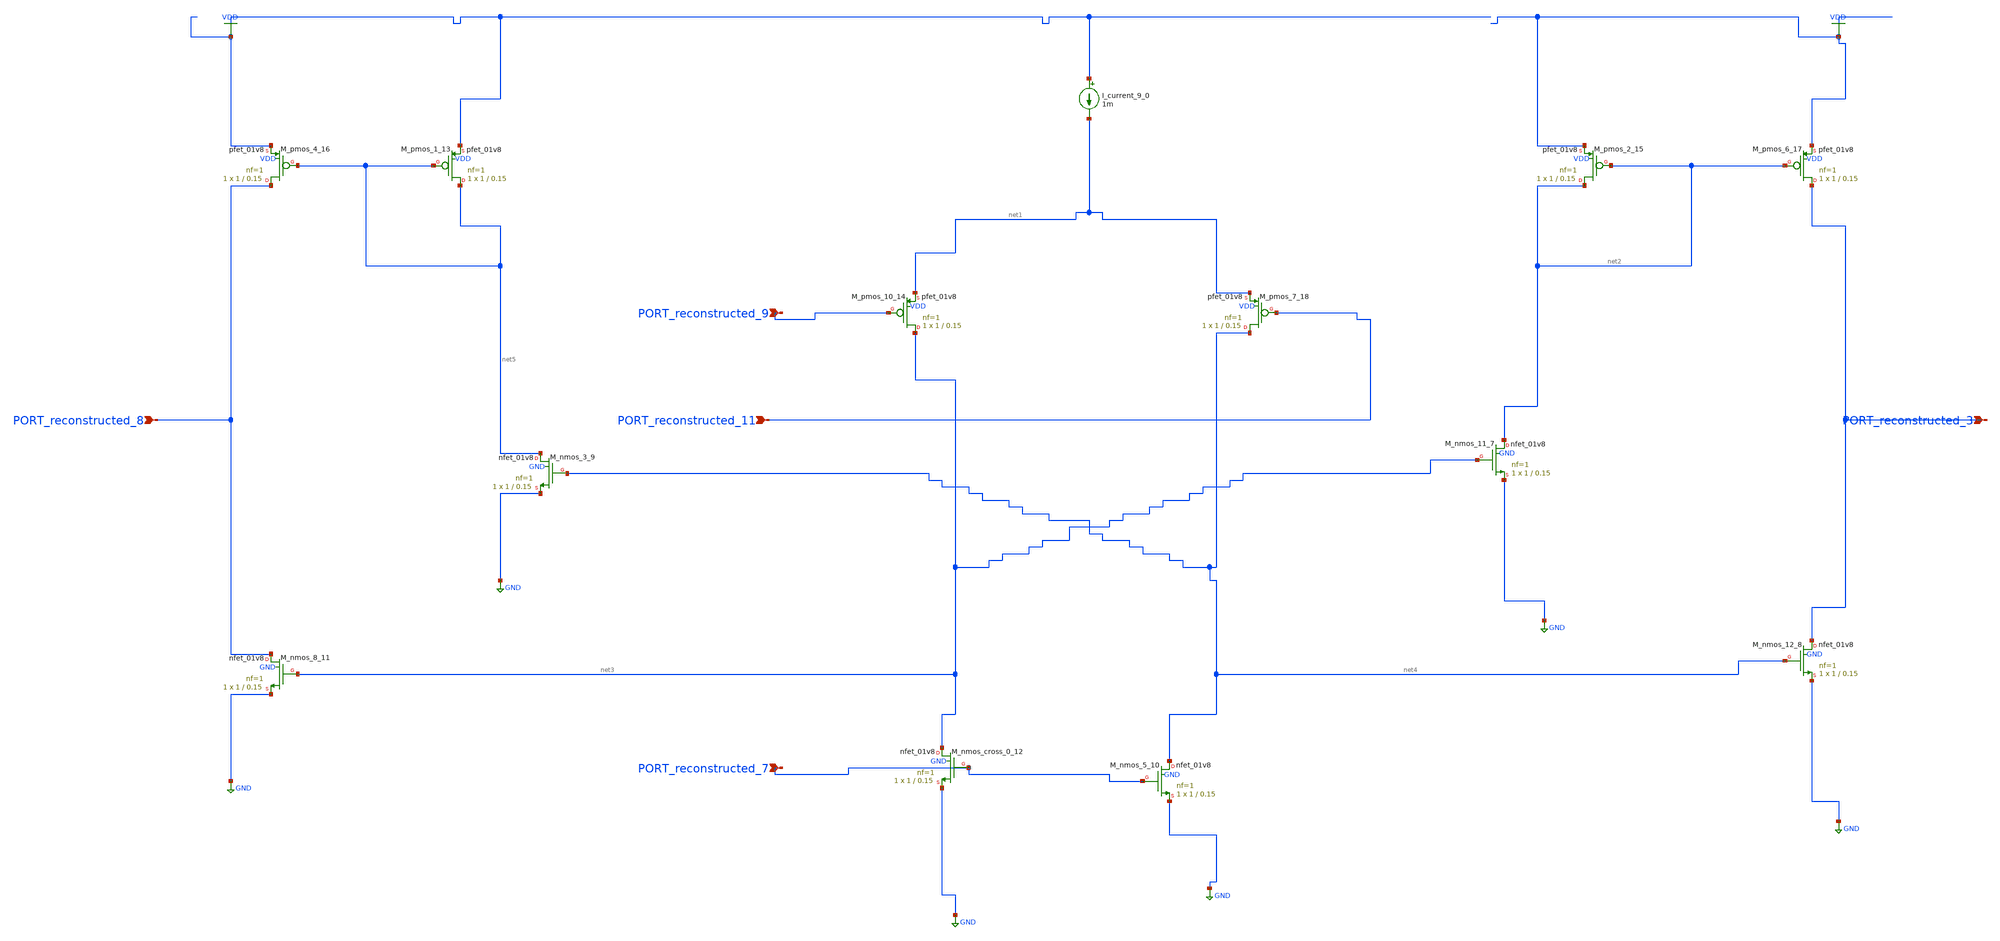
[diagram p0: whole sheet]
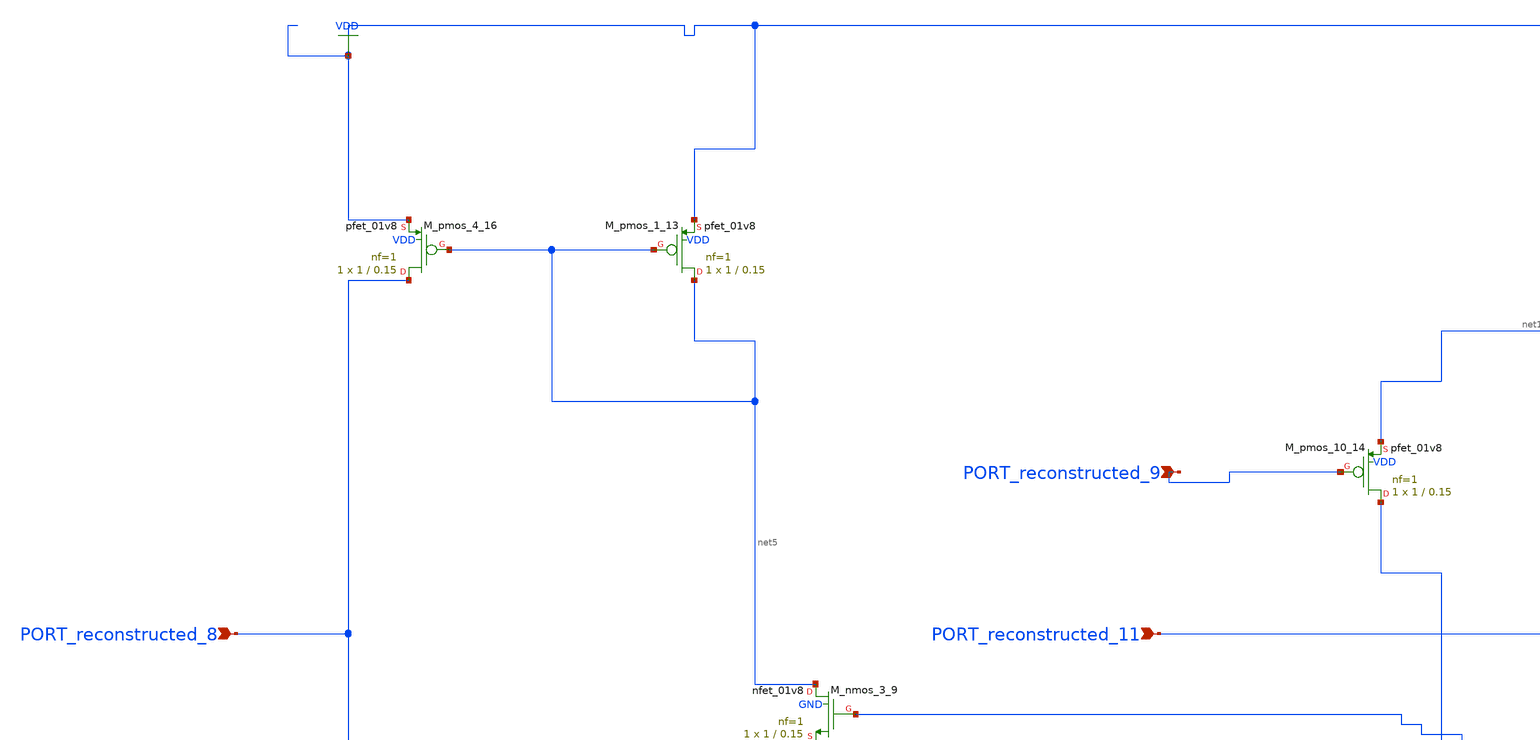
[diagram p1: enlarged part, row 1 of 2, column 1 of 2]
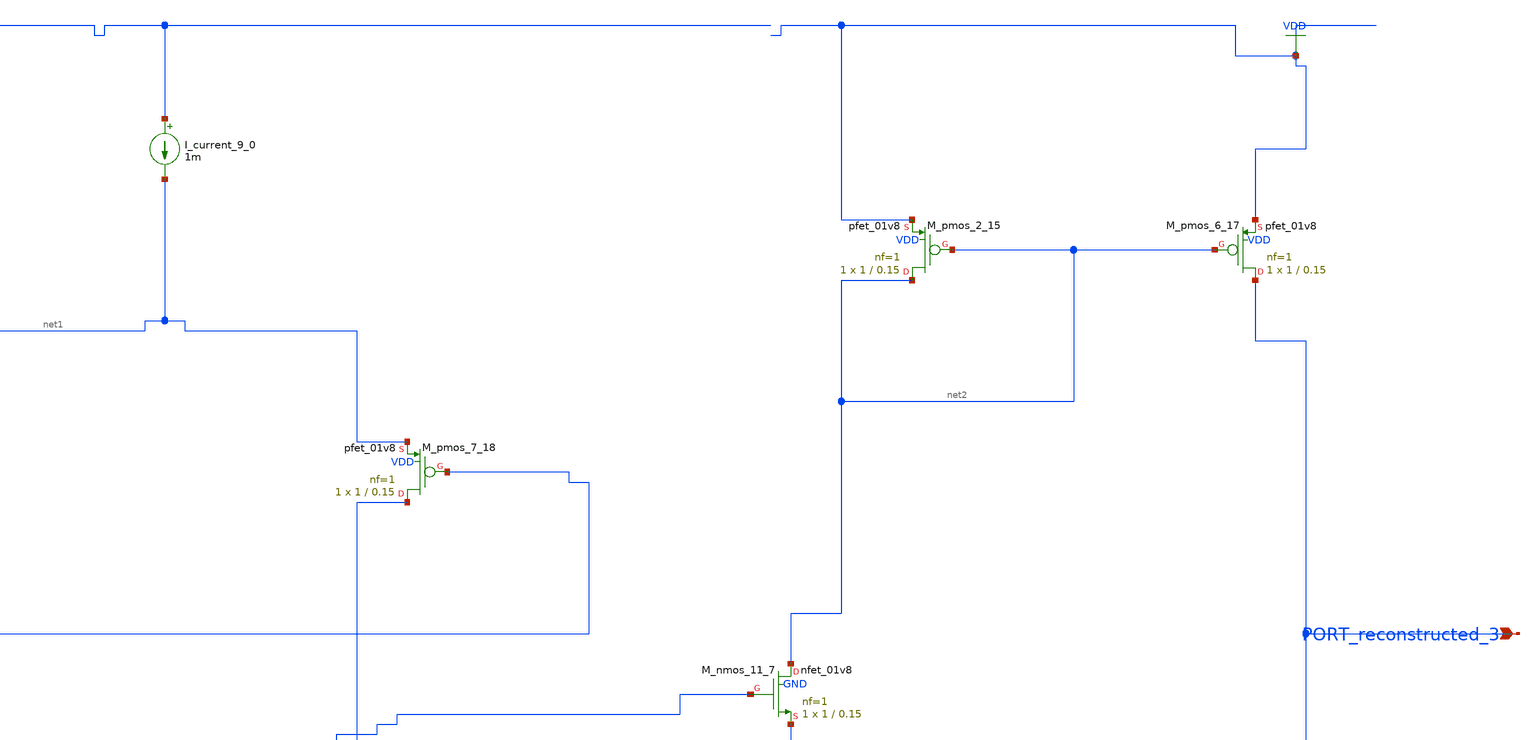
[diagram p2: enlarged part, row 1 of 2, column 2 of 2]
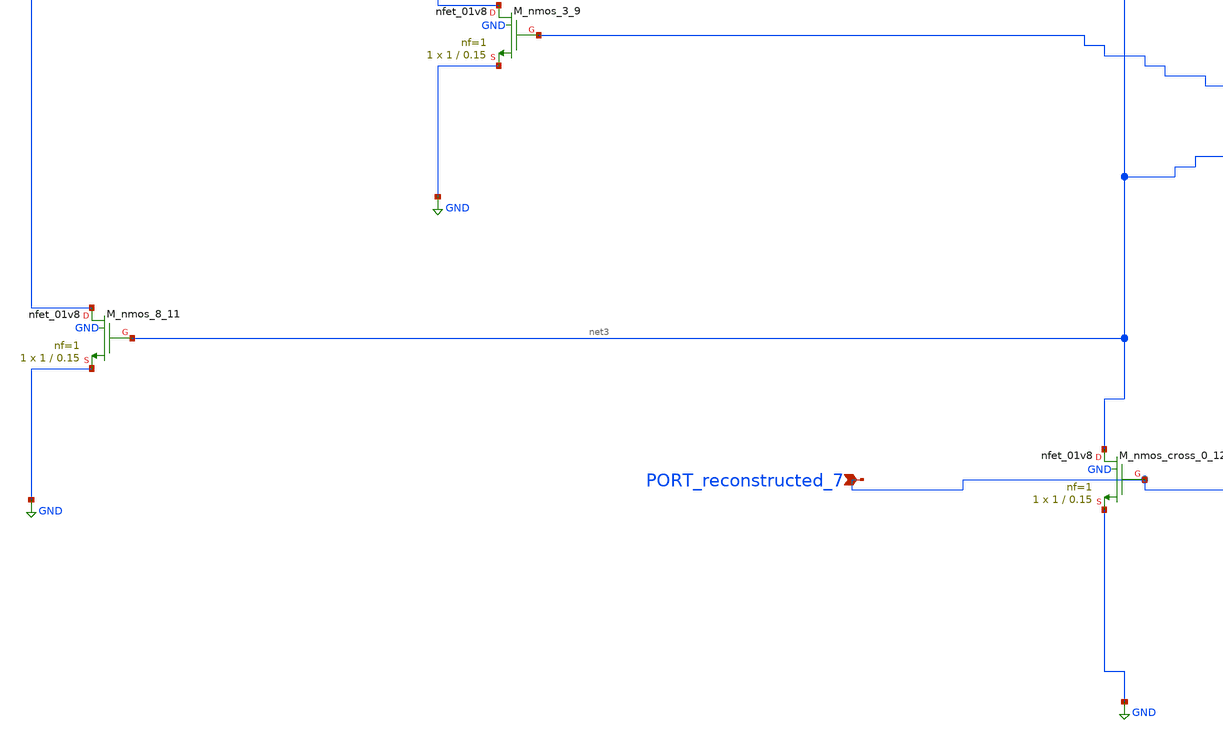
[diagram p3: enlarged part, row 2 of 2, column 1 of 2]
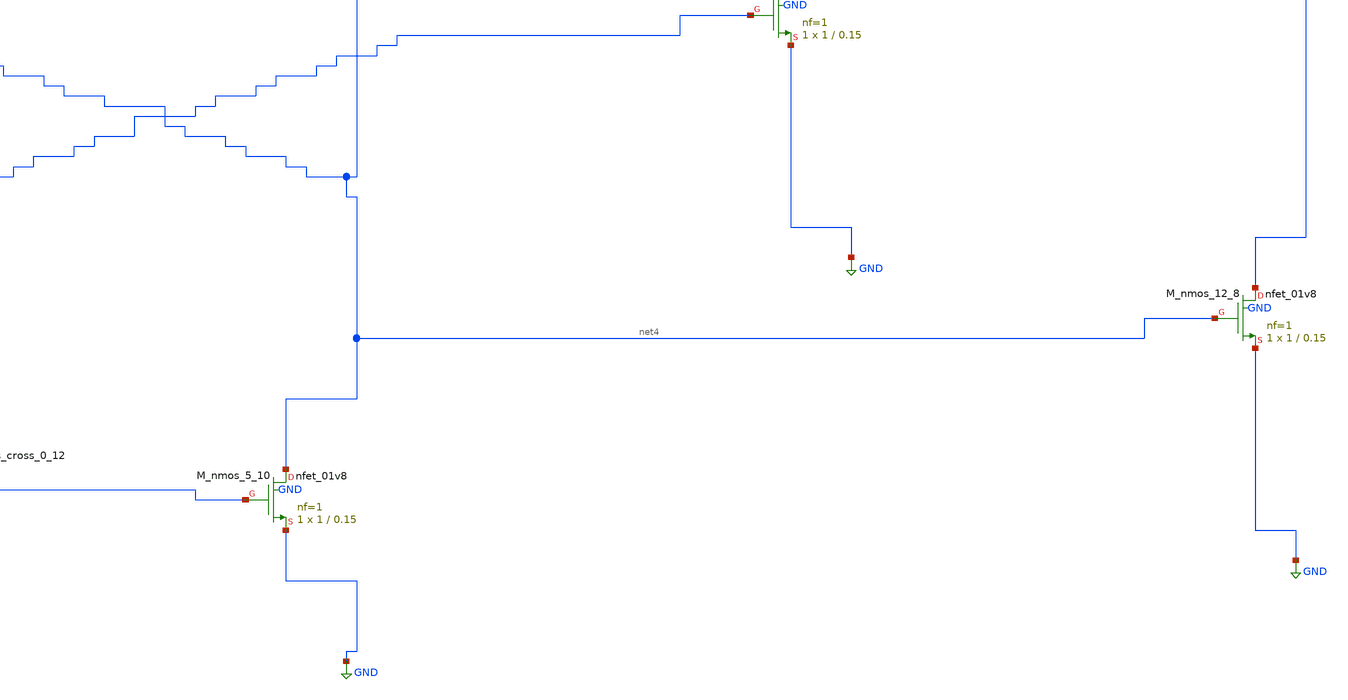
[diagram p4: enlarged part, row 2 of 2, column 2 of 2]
** sch_path: schematics/AMSNet/716.sch
**.subckt 716 PORT_reconstructed_3 PORT_reconstructed_8 PORT_reconstructed_9 PORT_reconstructed_7
*+ PORT_reconstructed_11
*.ipin PORT_reconstructed_3
*.ipin PORT_reconstructed_8
*.ipin PORT_reconstructed_9
*.ipin PORT_reconstructed_7
*.ipin PORT_reconstructed_11
I_current_9_0 VDD net1 1m
XM_nmos_11_7 net2 net3 GND GND sky130_fd_pr__nfet_01v8 L=0.15 W=1 nf=1 ad='int((1 + 1)/2) * 1 / 1 * 0.29'
+ as='int((1 + 2)/2) * 1 / 1 * 0.29' pd='2*int((1 + 1)/2) * (1 / 1 + 0.29)' ps='2*int((1 + 2)/2) * (1 / 1 + 0.29)'
+ nrd='0.29 / 1 ' nrs='0.29 / 1 ' sa=0 sb=0 sd=0 mult=1 m=1
XM_nmos_12_8 PORT_reconstructed_3 net4 GND GND sky130_fd_pr__nfet_01v8 L=0.15 W=1 nf=1 ad='int((1 + 1)/2) * 1 / 1 * 0.29'
+ as='int((1 + 2)/2) * 1 / 1 * 0.29' pd='2*int((1 + 1)/2) * (1 / 1 + 0.29)' ps='2*int((1 + 2)/2) * (1 / 1 + 0.29)'
+ nrd='0.29 / 1 ' nrs='0.29 / 1 ' sa=0 sb=0 sd=0 mult=1 m=1
XM_nmos_3_9 net5 net4 GND GND sky130_fd_pr__nfet_01v8 L=0.15 W=1 nf=1 ad='int((1 + 1)/2) * 1 / 1 * 0.29'
+ as='int((1 + 2)/2) * 1 / 1 * 0.29' pd='2*int((1 + 1)/2) * (1 / 1 + 0.29)' ps='2*int((1 + 2)/2) * (1 / 1 + 0.29)'
+ nrd='0.29 / 1 ' nrs='0.29 / 1 ' sa=0 sb=0 sd=0 mult=1 m=1
XM_nmos_5_10 net4 PORT_reconstructed_7 GND GND sky130_fd_pr__nfet_01v8 L=0.15 W=1 nf=1 ad='int((1 + 1)/2) * 1 / 1 * 0.29'
+ as='int((1 + 2)/2) * 1 / 1 * 0.29' pd='2*int((1 + 1)/2) * (1 / 1 + 0.29)' ps='2*int((1 + 2)/2) * (1 / 1 + 0.29)'
+ nrd='0.29 / 1 ' nrs='0.29 / 1 ' sa=0 sb=0 sd=0 mult=1 m=1
XM_nmos_8_11 PORT_reconstructed_8 net3 GND GND sky130_fd_pr__nfet_01v8 L=0.15 W=1 nf=1 ad='int((1 + 1)/2) * 1 / 1 * 0.29'
+ as='int((1 + 2)/2) * 1 / 1 * 0.29' pd='2*int((1 + 1)/2) * (1 / 1 + 0.29)' ps='2*int((1 + 2)/2) * (1 / 1 + 0.29)'
+ nrd='0.29 / 1 ' nrs='0.29 / 1 ' sa=0 sb=0 sd=0 mult=1 m=1
XM_nmos_cross_0_12 net3 PORT_reconstructed_7 GND GND sky130_fd_pr__nfet_01v8 L=0.15 W=1 nf=1 ad='int((1 + 1)/2) * 1 / 1 * 0.29'
+ as='int((1 + 2)/2) * 1 / 1 * 0.29' pd='2*int((1 + 1)/2) * (1 / 1 + 0.29)' ps='2*int((1 + 2)/2) * (1 / 1 + 0.29)'
+ nrd='0.29 / 1 ' nrs='0.29 / 1 ' sa=0 sb=0 sd=0 mult=1 m=1
XM_pmos_1_13 net5 net5 VDD VDD sky130_fd_pr__pfet_01v8 L=0.15 W=1 nf=1 ad='int((1 + 1)/2) * 1 / 1 * 0.29'
+ as='int((1 + 2)/2) * 1 / 1 * 0.29' pd='2*int((1 + 1)/2) * (1 / 1 + 0.29)' ps='2*int((1 + 2)/2) * (1 / 1 + 0.29)'
+ nrd='0.29 / 1 ' nrs='0.29 / 1 ' sa=0 sb=0 sd=0 mult=1 m=1
XM_pmos_10_14 net3 PORT_reconstructed_9 net1 VDD sky130_fd_pr__pfet_01v8 L=0.15 W=1 nf=1 ad='int((1 + 1)/2) * 1 / 1 * 0.29'
+ as='int((1 + 2)/2) * 1 / 1 * 0.29' pd='2*int((1 + 1)/2) * (1 / 1 + 0.29)' ps='2*int((1 + 2)/2) * (1 / 1 + 0.29)'
+ nrd='0.29 / 1 ' nrs='0.29 / 1 ' sa=0 sb=0 sd=0 mult=1 m=1
XM_pmos_2_15 net2 net2 VDD VDD sky130_fd_pr__pfet_01v8 L=0.15 W=1 nf=1 ad='int((1 + 1)/2) * 1 / 1 * 0.29'
+ as='int((1 + 2)/2) * 1 / 1 * 0.29' pd='2*int((1 + 1)/2) * (1 / 1 + 0.29)' ps='2*int((1 + 2)/2) * (1 / 1 + 0.29)'
+ nrd='0.29 / 1 ' nrs='0.29 / 1 ' sa=0 sb=0 sd=0 mult=1 m=1
XM_pmos_4_16 PORT_reconstructed_8 net5 VDD VDD sky130_fd_pr__pfet_01v8 L=0.15 W=1 nf=1 ad='int((1 + 1)/2) * 1 / 1 * 0.29'
+ as='int((1 + 2)/2) * 1 / 1 * 0.29' pd='2*int((1 + 1)/2) * (1 / 1 + 0.29)' ps='2*int((1 + 2)/2) * (1 / 1 + 0.29)'
+ nrd='0.29 / 1 ' nrs='0.29 / 1 ' sa=0 sb=0 sd=0 mult=1 m=1
XM_pmos_6_17 PORT_reconstructed_3 net2 VDD VDD sky130_fd_pr__pfet_01v8 L=0.15 W=1 nf=1 ad='int((1 + 1)/2) * 1 / 1 * 0.29'
+ as='int((1 + 2)/2) * 1 / 1 * 0.29' pd='2*int((1 + 1)/2) * (1 / 1 + 0.29)' ps='2*int((1 + 2)/2) * (1 / 1 + 0.29)'
+ nrd='0.29 / 1 ' nrs='0.29 / 1 ' sa=0 sb=0 sd=0 mult=1 m=1
XM_pmos_7_18 net4 PORT_reconstructed_11 net1 VDD sky130_fd_pr__pfet_01v8 L=0.15 W=1 nf=1 ad='int((1 + 1)/2) * 1 / 1 * 0.29'
+ as='int((1 + 2)/2) * 1 / 1 * 0.29' pd='2*int((1 + 1)/2) * (1 / 1 + 0.29)' ps='2*int((1 + 2)/2) * (1 / 1 + 0.29)'
+ nrd='0.29 / 1 ' nrs='0.29 / 1 ' sa=0 sb=0 sd=0 mult=1 m=1
**.ends
.GLOBAL GND
.GLOBAL VDD
.end
